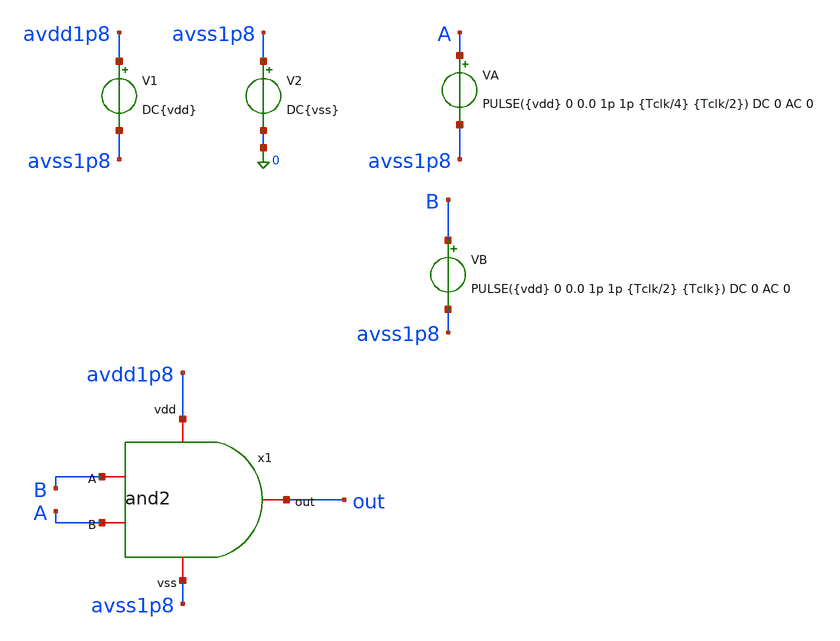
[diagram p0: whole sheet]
** sch_path: verification/testbenches/tb_and2.sch
**.subckt tb_and2
V1 avdd1p8 avss1p8 DC{vdd}
V2 avss1p8 0 DC{vss}
VA A avss1p8 PULSE({vdd} 0 0.0 1p 1p {Tclk/4} {Tclk/2}) DC 0 AC 0
VB B avss1p8 PULSE({vdd} 0 0.0 1p 1p {Tclk/2} {Tclk}) DC 0 AC 0
x1 avdd1p8 B out A avss1p8 and2
**** begin user architecture code


* Circuit Parameters
.param vdd = 1.2
.param vss = 0.0
.param Tclk = 10n
.options TEMP = 27.0
* Include Models - IHP SG13G2
.lib cornerMOSlv.lib mos_tt
* OP Parameters & Singals to save
.save all
*Simulations
.control
tran 0.01u 100n
setplot tran1
plot v(A) v(B)+1.2 v(out)+3
reset
.endc
.end


**** end user architecture code
**.ends

* expanding   symbol:  blocks/and2/schematic/and2.sym # of pins=5
** sym_path: design/blocks/and2/schematic/and2.sym
** sch_path: design/blocks/and2/schematic/and2.sch
.subckt and2 vdd A out B vss
*.iopin A
*.iopin B
*.iopin vss
*.iopin vdd
*.iopin out
X2 net1 A net2 vss sg13_lv_nmos w=1.5u l=0.15u ng=1 m=1 mm_ok=1
X0 net1 A vdd vdd sg13_lv_pmos w=1.5u l=0.15u ng=1 m=1 mm_ok=1
X3 net2 B vss vss sg13_lv_nmos w=1.5u l=0.15u ng=1 m=1 mm_ok=1
X1 net1 B vdd vdd sg13_lv_pmos w=0.15u l=0.13u ng=1 m=1 mm_ok=1
X4 out net1 vdd vdd sg13_lv_pmos w=1.5u l=0.15u ng=1 m=1 mm_ok=1
X5 out net1 vss vss sg13_lv_nmos w=.75u l=0.15u ng=1 m=1 mm_ok=1
.ends

.end
